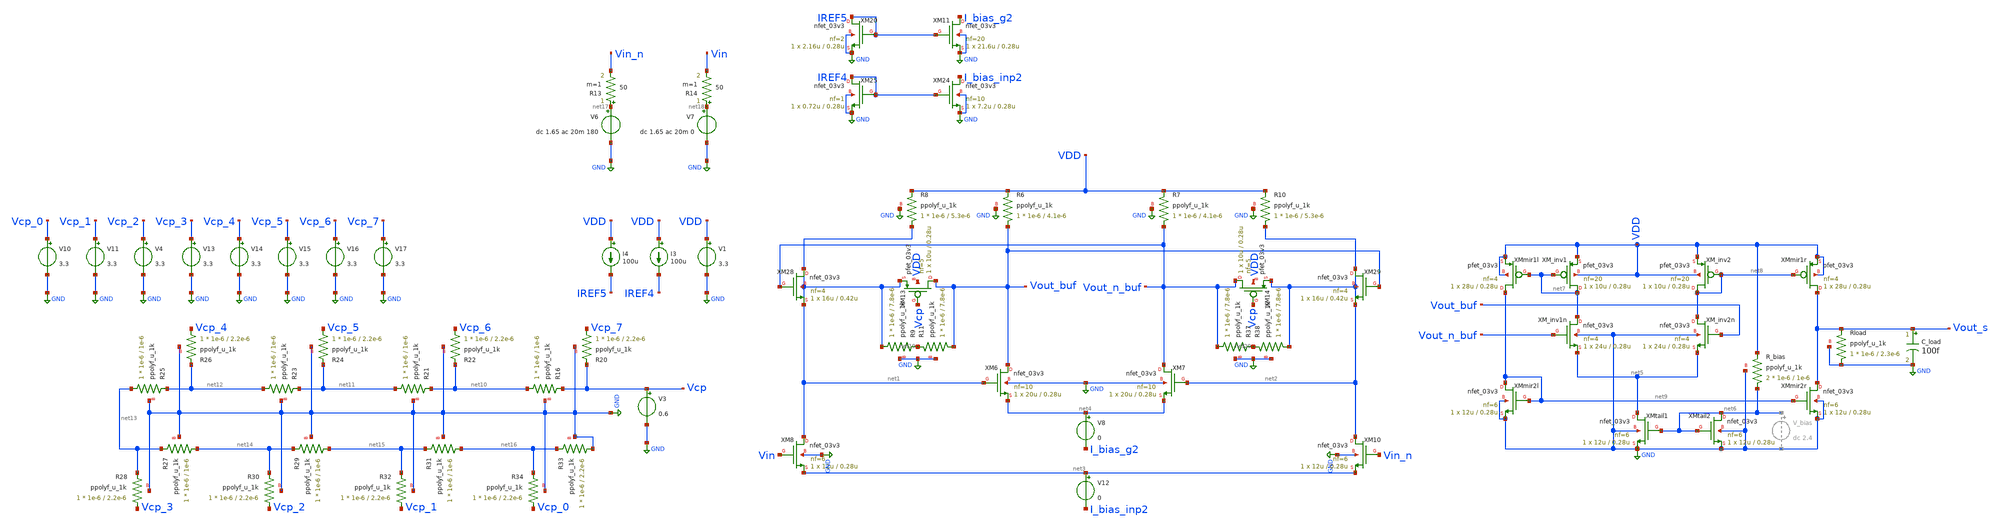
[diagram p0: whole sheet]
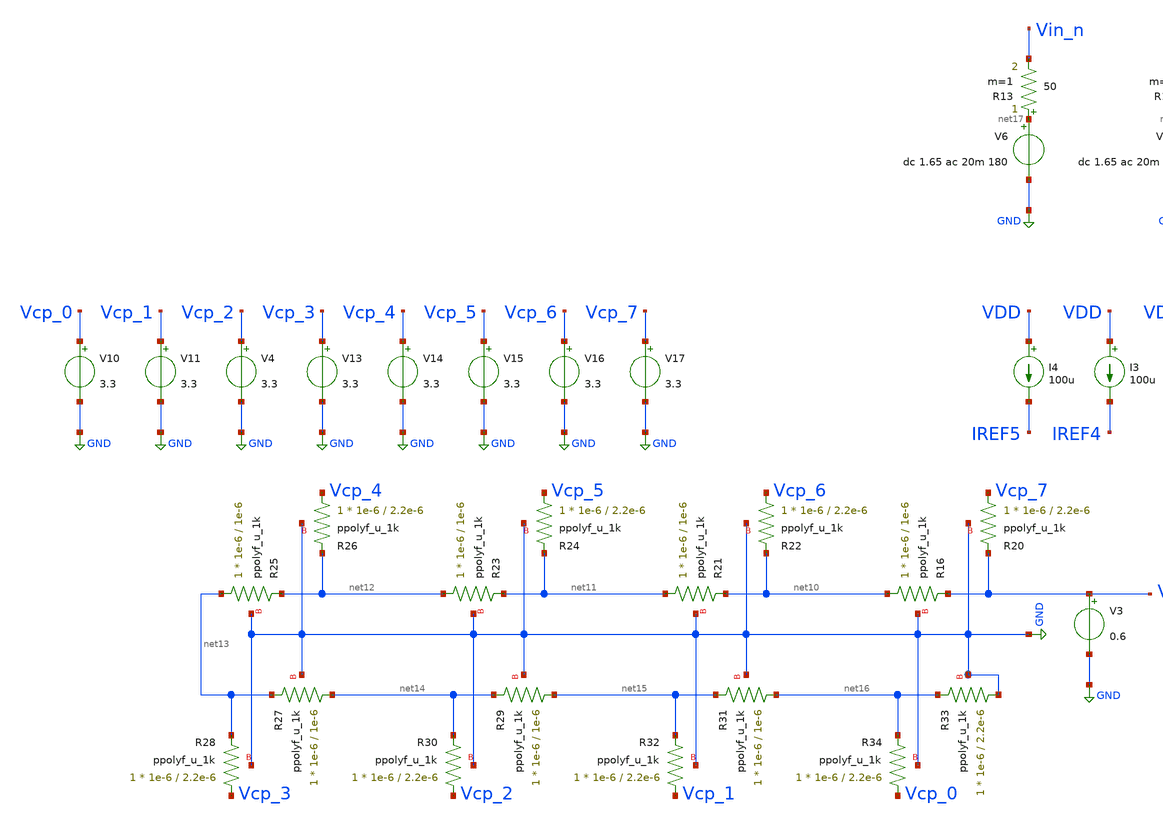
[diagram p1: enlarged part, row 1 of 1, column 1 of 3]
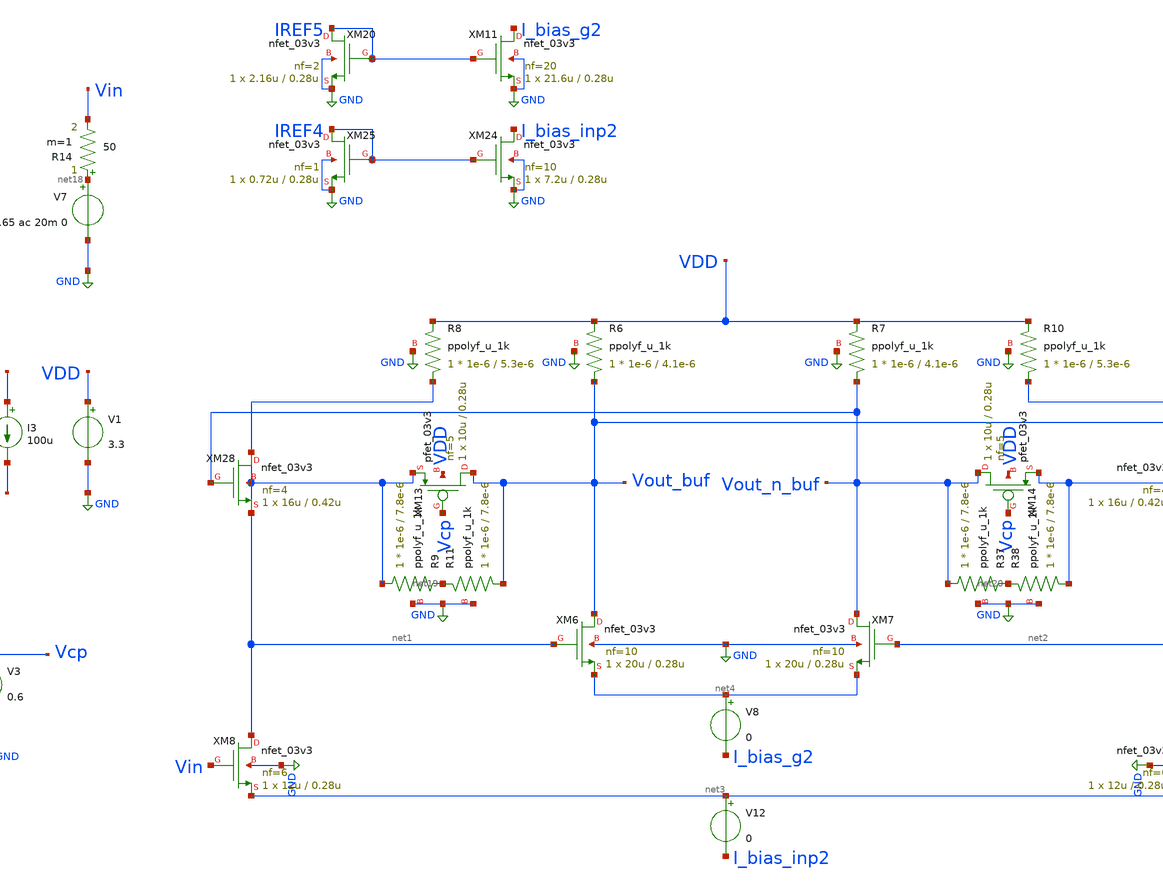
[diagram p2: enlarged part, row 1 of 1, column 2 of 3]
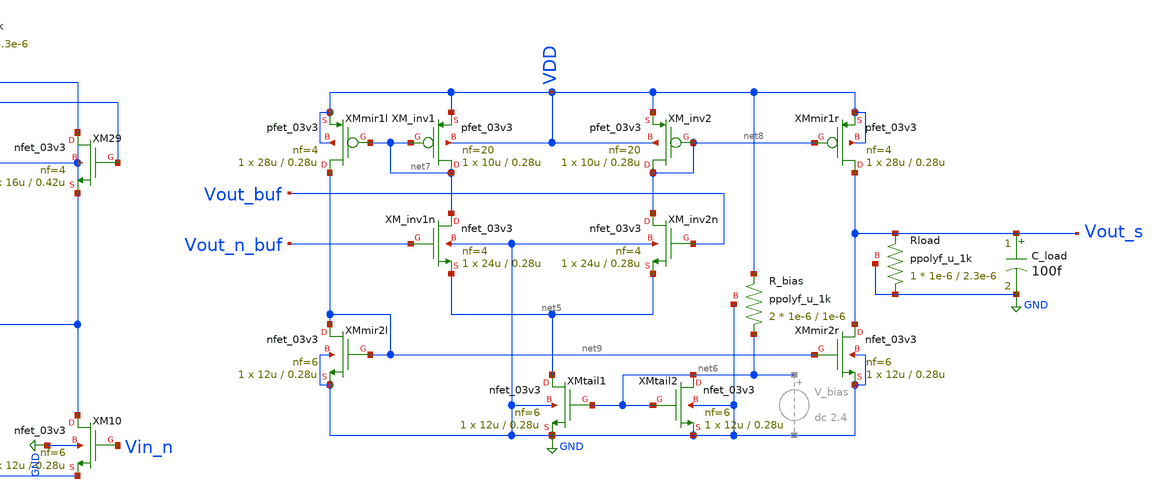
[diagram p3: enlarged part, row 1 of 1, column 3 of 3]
** sch_path: blocks/vga/vga.sch
**.subckt vga
V1 VDD GND 3.3
V6 net17 GND dc 1.65 ac 20m 180
XM6 Vout_buf net1 net4 GND nfet_03v3 L=0.28u W=20u nf=10 ad='int((nf+1)/2) * W/nf * 0.18u' as='int((nf+2)/2) * W/nf * 0.18u'
+ pd='2*int((nf+1)/2) * (W/nf + 0.18u)' ps='2*int((nf+2)/2) * (W/nf + 0.18u)' nrd='0.18u / W' nrs='0.18u / W'
+ sa=0 sb=0 sd=0 m=1
XM7 Vout_n_buf net2 net4 GND nfet_03v3 L=0.28u W=20u nf=10 ad='int((nf+1)/2) * W/nf * 0.18u' as='int((nf+2)/2) * W/nf * 0.18u'
+ pd='2*int((nf+1)/2) * (W/nf + 0.18u)' ps='2*int((nf+2)/2) * (W/nf + 0.18u)' nrd='0.18u / W' nrs='0.18u / W'
+ sa=0 sb=0 sd=0 m=1
XM8 net1 Vin net3 GND nfet_03v3 L=0.28u W=12u nf=6 ad='int((nf+1)/2) * W/nf * 0.18u' as='int((nf+2)/2) * W/nf * 0.18u'
+ pd='2*int((nf+1)/2) * (W/nf + 0.18u)' ps='2*int((nf+2)/2) * (W/nf + 0.18u)' nrd='0.18u / W' nrs='0.18u / W'
+ sa=0 sb=0 sd=0 m=1
XM10 net2 Vin_n net3 GND nfet_03v3 L=0.28u W=12u nf=6 ad='int((nf+1)/2) * W/nf * 0.18u' as='int((nf+2)/2) * W/nf * 0.18u'
+ pd='2*int((nf+1)/2) * (W/nf + 0.18u)' ps='2*int((nf+2)/2) * (W/nf + 0.18u)' nrd='0.18u / W' nrs='0.18u / W'
+ sa=0 sb=0 sd=0 m=1
V7 net18 GND dc 1.65 ac 20m 0
R14 net18 Vin 50 m=1
R13 net17 Vin_n 50 m=1
XM28 net1 Vout_n_buf net1 net1 nfet_03v3 L=0.42u W=16u nf=4 ad='int((nf+1)/2) * W/nf * 0.18u' as='int((nf+2)/2) * W/nf * 0.18u'
+ pd='2*int((nf+1)/2) * (W/nf + 0.18u)' ps='2*int((nf+2)/2) * (W/nf + 0.18u)' nrd='0.18u / W' nrs='0.18u / W'
+ sa=0 sb=0 sd=0 m=1
XM29 net2 Vout_buf net2 net2 nfet_03v3 L=0.42u W=16u nf=4 ad='int((nf+1)/2) * W/nf * 0.18u' as='int((nf+2)/2) * W/nf * 0.18u'
+ pd='2*int((nf+1)/2) * (W/nf + 0.18u)' ps='2*int((nf+2)/2) * (W/nf + 0.18u)' nrd='0.18u / W' nrs='0.18u / W'
+ sa=0 sb=0 sd=0 m=1
XM_inv1 net7 net7 VDD VDD pfet_03v3 L=0.28u W=10u nf=20 ad='int((nf+1)/2) * W/nf * 0.18u' as='int((nf+2)/2) * W/nf * 0.18u'
+ pd='2*int((nf+1)/2) * (W/nf + 0.18u)' ps='2*int((nf+2)/2) * (W/nf + 0.18u)' nrd='0.18u / W' nrs='0.18u / W'
+ sa=0 sb=0 sd=0 m=1
XM_inv1n net7 Vout_n_buf net5 GND nfet_03v3 L=0.28u W=24u nf=4 ad='int((nf+1)/2) * W/nf * 0.18u' as='int((nf+2)/2) * W/nf * 0.18u'
+ pd='2*int((nf+1)/2) * (W/nf + 0.18u)' ps='2*int((nf+2)/2) * (W/nf + 0.18u)' nrd='0.18u / W' nrs='0.18u / W'
+ sa=0 sb=0 sd=0 m=1
XM_inv2 net8 net8 VDD VDD pfet_03v3 L=0.28u W=10u nf=20 ad='int((nf+1)/2) * W/nf * 0.18u' as='int((nf+2)/2) * W/nf * 0.18u'
+ pd='2*int((nf+1)/2) * (W/nf + 0.18u)' ps='2*int((nf+2)/2) * (W/nf + 0.18u)' nrd='0.18u / W' nrs='0.18u / W'
+ sa=0 sb=0 sd=0 m=1
XM_inv2n net8 Vout_buf net5 GND nfet_03v3 L=0.28u W=24u nf=4 ad='int((nf+1)/2) * W/nf * 0.18u' as='int((nf+2)/2) * W/nf * 0.18u'
+ pd='2*int((nf+1)/2) * (W/nf + 0.18u)' ps='2*int((nf+2)/2) * (W/nf + 0.18u)' nrd='0.18u / W' nrs='0.18u / W'
+ sa=0 sb=0 sd=0 m=1
XMtail1 net5 net6 GND GND nfet_03v3 L=0.28u W=12u nf=6 ad='int((nf+1)/2) * W/nf * 0.18u' as='int((nf+2)/2) * W/nf * 0.18u'
+ pd='2*int((nf+1)/2) * (W/nf + 0.18u)' ps='2*int((nf+2)/2) * (W/nf + 0.18u)' nrd='0.18u / W' nrs='0.18u / W'
+ sa=0 sb=0 sd=0 m=1
XMtail2 net6 net6 GND GND nfet_03v3 L=0.28u W=12u nf=6 ad='int((nf+1)/2) * W/nf * 0.18u' as='int((nf+2)/2) * W/nf * 0.18u'
+ pd='2*int((nf+1)/2) * (W/nf + 0.18u)' ps='2*int((nf+2)/2) * (W/nf + 0.18u)' nrd='0.18u / W' nrs='0.18u / W'
+ sa=0 sb=0 sd=0 m=1
XMmir1l net9 net7 VDD VDD pfet_03v3 L=0.28u W=28u nf=4 ad='int((nf+1)/2) * W/nf * 0.18u' as='int((nf+2)/2) * W/nf * 0.18u'
+ pd='2*int((nf+1)/2) * (W/nf + 0.18u)' ps='2*int((nf+2)/2) * (W/nf + 0.18u)' nrd='0.18u / W' nrs='0.18u / W'
+ sa=0 sb=0 sd=0 m=1
XMmir1r Vout_s net8 VDD VDD pfet_03v3 L=0.28u W=28u nf=4 ad='int((nf+1)/2) * W/nf * 0.18u' as='int((nf+2)/2) * W/nf * 0.18u'
+ pd='2*int((nf+1)/2) * (W/nf + 0.18u)' ps='2*int((nf+2)/2) * (W/nf + 0.18u)' nrd='0.18u / W' nrs='0.18u / W'
+ sa=0 sb=0 sd=0 m=1
XMmir2l net9 net9 GND GND nfet_03v3 L=0.28u W=12u nf=6 ad='int((nf+1)/2) * W/nf * 0.18u' as='int((nf+2)/2) * W/nf * 0.18u'
+ pd='2*int((nf+1)/2) * (W/nf + 0.18u)' ps='2*int((nf+2)/2) * (W/nf + 0.18u)' nrd='0.18u / W' nrs='0.18u / W'
+ sa=0 sb=0 sd=0 m=1
XMmir2r Vout_s net9 GND GND nfet_03v3 L=0.28u W=12u nf=6 ad='int((nf+1)/2) * W/nf * 0.18u' as='int((nf+2)/2) * W/nf * 0.18u'
+ pd='2*int((nf+1)/2) * (W/nf + 0.18u)' ps='2*int((nf+2)/2) * (W/nf + 0.18u)' nrd='0.18u / W' nrs='0.18u / W'
+ sa=0 sb=0 sd=0 m=1
XR_bias net6 VDD GND ppolyf_u_1k r_width=1e-6 r_length=1e-6 m=2
C_load Vout_s GND 100f m=1
XR16 net10 Vcp GND ppolyf_u_1k r_width=1e-6 r_length=1e-6 m=1
XR20 Vcp_7 Vcp GND ppolyf_u_1k r_width=1e-6 r_length=2.2e-6 m=1
XR21 net11 net10 GND ppolyf_u_1k r_width=1e-6 r_length=1e-6 m=1
XR22 Vcp_6 net10 GND ppolyf_u_1k r_width=1e-6 r_length=2.2e-6 m=1
XR23 net12 net11 GND ppolyf_u_1k r_width=1e-6 r_length=1e-6 m=1
XR24 Vcp_5 net11 GND ppolyf_u_1k r_width=1e-6 r_length=2.2e-6 m=1
XR25 net13 net12 GND ppolyf_u_1k r_width=1e-6 r_length=1e-6 m=1
XR26 Vcp_4 net12 GND ppolyf_u_1k r_width=1e-6 r_length=2.2e-6 m=1
XR27 net14 net13 GND ppolyf_u_1k r_width=1e-6 r_length=1e-6 m=1
XR28 Vcp_3 net13 GND ppolyf_u_1k r_width=1e-6 r_length=2.2e-6 m=1
XR29 net15 net14 GND ppolyf_u_1k r_width=1e-6 r_length=1e-6 m=1
XR30 Vcp_2 net14 GND ppolyf_u_1k r_width=1e-6 r_length=2.2e-6 m=1
XR31 net16 net15 GND ppolyf_u_1k r_width=1e-6 r_length=1e-6 m=1
XR32 Vcp_1 net15 GND ppolyf_u_1k r_width=1e-6 r_length=2.2e-6 m=1
XR33 GND net16 GND ppolyf_u_1k r_width=1e-6 r_length=2.2e-6 m=1
XR34 Vcp_0 net16 GND ppolyf_u_1k r_width=1e-6 r_length=2.2e-6 m=1
V10 Vcp_0 GND 3.3
V11 Vcp_1 GND 3.3
V4 Vcp_2 GND 3.3
V13 Vcp_3 GND 3.3
V14 Vcp_4 GND 3.3
V15 Vcp_5 GND 3.3
V16 Vcp_6 GND 3.3
V17 Vcp_7 GND 3.3
V3 Vcp GND 0.6
XM13 Vout_buf Vcp net1 VDD pfet_03v3 L=0.28u W=10u nf=5 ad='int((nf+1)/2) * W/nf * 0.18u' as='int((nf+2)/2) * W/nf * 0.18u'
+ pd='2*int((nf+1)/2) * (W/nf + 0.18u)' ps='2*int((nf+2)/2) * (W/nf + 0.18u)' nrd='0.18u / W' nrs='0.18u / W'
+ sa=0 sb=0 sd=0 m=1
XR9 net1 net19 GND ppolyf_u_1k r_width=1e-6 r_length=7.8e-6 m=1
XR11 Vout_buf net19 GND ppolyf_u_1k r_width=1e-6 r_length=7.8e-6 m=1
XM14 Vout_n_buf Vcp net2 VDD pfet_03v3 L=0.28u W=10u nf=5 ad='int((nf+1)/2) * W/nf * 0.18u' as='int((nf+2)/2) * W/nf * 0.18u'
+ pd='2*int((nf+1)/2) * (W/nf + 0.18u)' ps='2*int((nf+2)/2) * (W/nf + 0.18u)' nrd='0.18u / W' nrs='0.18u / W'
+ sa=0 sb=0 sd=0 m=1
XR37 Vout_n_buf net20 GND ppolyf_u_1k r_width=1e-6 r_length=7.8e-6 m=1
XR38 net2 net20 GND ppolyf_u_1k r_width=1e-6 r_length=7.8e-6 m=1
XRload GND Vout_s GND ppolyf_u_1k r_width=1e-6 r_length=2.3e-6 m=1
XR6 Vout_buf VDD GND ppolyf_u_1k r_width=1e-6 r_length=4.1e-6 m=1
XR7 Vout_n_buf VDD GND ppolyf_u_1k r_width=1e-6 r_length=4.1e-6 m=1
XR8 net1 VDD GND ppolyf_u_1k r_width=1e-6 r_length=5.3e-6 m=1
XR10 net2 VDD GND ppolyf_u_1k r_width=1e-6 r_length=5.3e-6 m=1
XM11 I_bias_g2 IREF5 GND GND nfet_03v3 L=0.28u W=21.6u nf=20 ad='int((nf+1)/2) * W/nf * 0.18u' as='int((nf+2)/2) * W/nf * 0.18u'
+ pd='2*int((nf+1)/2) * (W/nf + 0.18u)' ps='2*int((nf+2)/2) * (W/nf + 0.18u)' nrd='0.18u / W' nrs='0.18u / W'
+ sa=0 sb=0 sd=0 m=1
XM20 IREF5 IREF5 GND GND nfet_03v3 L=0.28u W=2.16u nf=2 ad='int((nf+1)/2) * W/nf * 0.18u' as='int((nf+2)/2) * W/nf * 0.18u'
+ pd='2*int((nf+1)/2) * (W/nf + 0.18u)' ps='2*int((nf+2)/2) * (W/nf + 0.18u)' nrd='0.18u / W' nrs='0.18u / W'
+ sa=0 sb=0 sd=0 m=1
V8 net4 I_bias_g2 0
I3 VDD IREF4 100u
XM24 I_bias_inp2 IREF4 GND GND nfet_03v3 L=0.28u W=7.2u nf=10 ad='int((nf+1)/2) * W/nf * 0.18u' as='int((nf+2)/2) * W/nf * 0.18u'
+ pd='2*int((nf+1)/2) * (W/nf + 0.18u)' ps='2*int((nf+2)/2) * (W/nf + 0.18u)' nrd='0.18u / W' nrs='0.18u / W'
+ sa=0 sb=0 sd=0 m=1
XM25 IREF4 IREF4 GND GND nfet_03v3 L=0.28u W=0.72u nf=1 ad='int((nf+1)/2) * W/nf * 0.18u' as='int((nf+2)/2) * W/nf * 0.18u'
+ pd='2*int((nf+1)/2) * (W/nf + 0.18u)' ps='2*int((nf+2)/2) * (W/nf + 0.18u)' nrd='0.18u / W' nrs='0.18u / W'
+ sa=0 sb=0 sd=0 m=1
I4 VDD IREF5 100u
V12 net3 I_bias_inp2 0
**** begin user architecture code


.include /foss/pdks/gf180mcuD/libs.tech/ngspice/design.ngspice
.lib /foss/pdks/gf180mcuD/libs.tech/ngspice/sm141064.ngspice ss
.lib /foss/pdks/gf180mcuD/libs.tech/ngspice/sm141064.ngspice bjt_ss
.lib /foss/pdks/gf180mcuD/libs.tech/ngspice/sm141064.ngspice diode_ss
.lib /foss/pdks/gf180mcuD/libs.tech/ngspice/sm141064.ngspice res_ss
.lib /foss/pdks/gf180mcuD/libs.tech/ngspice/sm141064.ngspice mimcap_ss
.lib /foss/pdks/gf180mcuD/libs.tech/ngspice/sm141064.ngspice moscap_ss
.option method=gear

.control
set temp = 25
  * 1. Setup the sweep parameters
  let v_ctrl = 0.6

  let f_start = 1
  let f_stop = 3.2G
  let f_points = 120

  * 2. Initialize vectors to store results
  let gain_db = unitvec(f_points)

  alter v3 = v_ctrl
  ac dec $&f_points $&f_start $&f_stop

  * 4. Calculate Differential Gain in dB
  * Formula: 20 * log10(|Vout_diff| / |Vin_diff|)
  let vin_mag = mag(v(vin) - v(vin_n))
  let vout_s_mag = mag(v(vout_s))
  let vout_buf_mag = mag(v(vout_buf) - v(vout_n_buf))
  let vout_s_gain = 20 * log10(vout_s_mag / vin_mag)
  let vout_buf_gain = 20 * log10(vout_buf_mag / vin_mag)

  * Credit to marcel hendrix
  * https://sourceforge.net/p/ngspice/discussion/133842/thread/2031ad61/
  meas ac peak  MAX  vmag(vout_s) FROM=$&f_start TO=$&f_stop
  let f3db = peak/sqrt(2)
  meas ac lo_3db WHEN vmag(vout_s)=f3db RISE=1
  meas ac hi_3db WHEN vmag(vout_s)=f3db FALL=1

  * 5. Save results to vectors
  plot vout_s_gain vout_buf_gain title 'Gain (dB) vs. Frequency from 1MHz to 3.2GHz, 0.6 vctrl' ylimit
+ 0 80
.endc


**** end user architecture code
**.ends
.GLOBAL GND
.end
